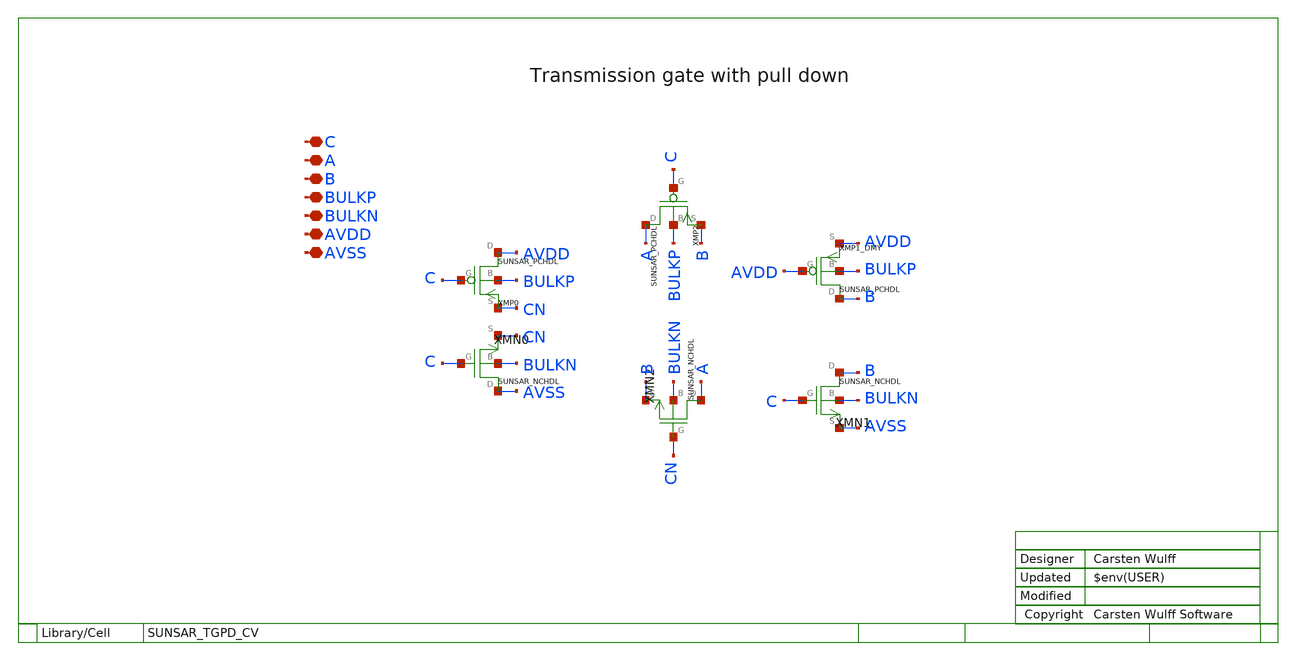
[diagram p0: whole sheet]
** sch_path: ip/sun_sar9b_sky130nm/design/SUN_SAR9B_SKY130NM/SUNSAR_TGPD_CV.sch
**.subckt SUNSAR_TGPD_CV C A B BULKP BULKN AVDD AVSS
*.iopin C
*.iopin A
*.iopin B
*.iopin BULKP
*.iopin BULKN
*.iopin AVDD
*.iopin AVSS
XMN0 AVSS C CN BULKN SUNSAR_NCHDL
XMN1 B C AVSS BULKN SUNSAR_NCHDL
XMN2 A CN B BULKN SUNSAR_NCHDL
XMP0 AVDD C CN BULKP SUNSAR_PCHDL
XMP1_DMY B AVDD AVDD BULKP SUNSAR_PCHDL
XMP2 A C B BULKP SUNSAR_PCHDL
**.ends
.end
